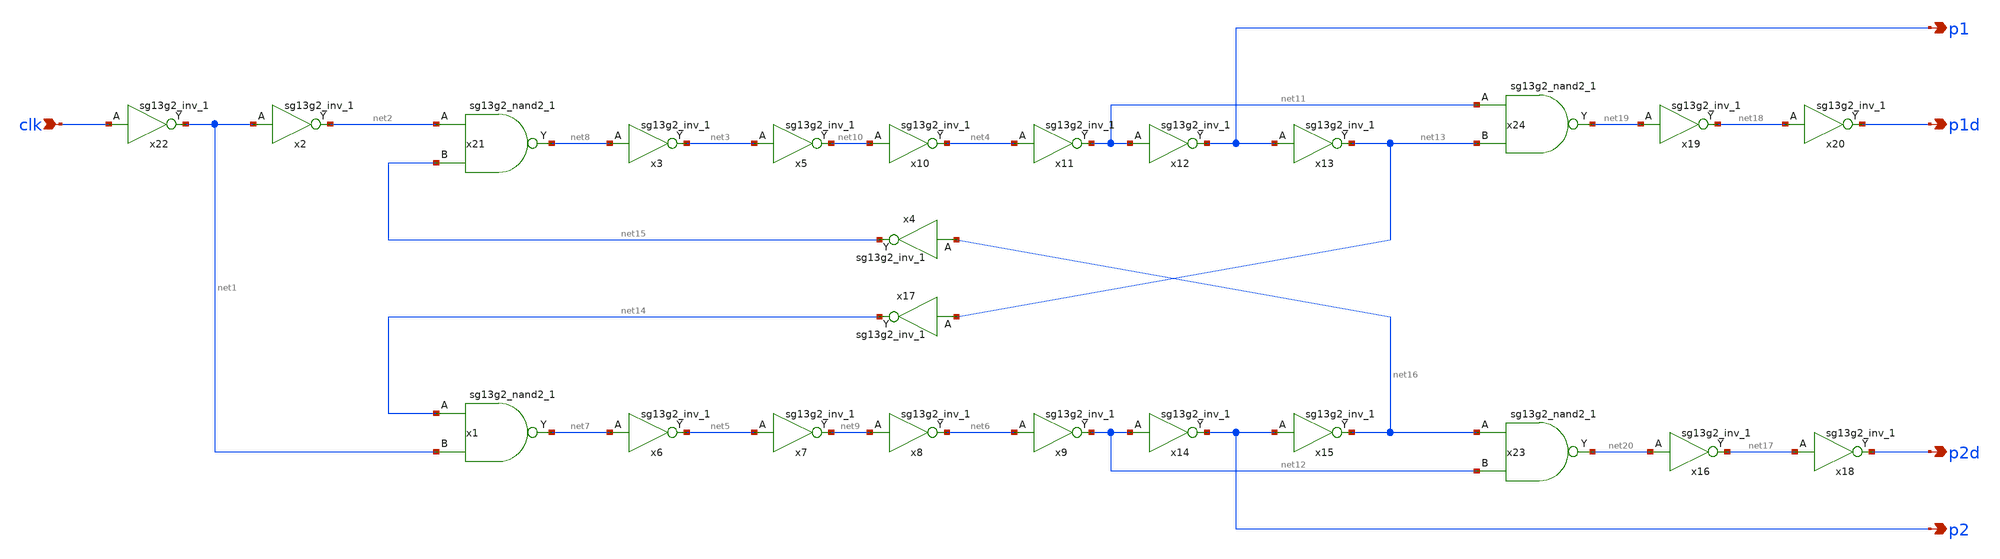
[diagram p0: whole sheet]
** sch_path: design/design_clkgen/clkgen.sch
**.subckt clkgen clk p1 p1d p2d p2
*.ipin clk
*.opin p1
*.opin p1d
*.opin p2d
*.opin p2
x21 net8 net2 net15 VDD VSS sg13g2_nand2_1
x22 net1 clk VDD VSS sg13g2_inv_1
x2 net2 net1 VDD VSS sg13g2_inv_1
x3 net3 net8 VDD VSS sg13g2_inv_1
x5 net10 net3 VDD VSS sg13g2_inv_1
x6 net5 net7 VDD VSS sg13g2_inv_1
x7 net9 net5 VDD VSS sg13g2_inv_1
x8 net6 net9 VDD VSS sg13g2_inv_1
x9 net12 net6 VDD VSS sg13g2_inv_1
x10 net4 net10 VDD VSS sg13g2_inv_1
x11 net11 net4 VDD VSS sg13g2_inv_1
x12 p1 net11 VDD VSS sg13g2_inv_1
x13 net13 p1 VDD VSS sg13g2_inv_1
x14 p2 net12 VDD VSS sg13g2_inv_1
x15 net16 p2 VDD VSS sg13g2_inv_1
x16 net17 net20 VDD VSS sg13g2_inv_1
x18 p2d net17 VDD VSS sg13g2_inv_1
x19 net18 net19 VDD VSS sg13g2_inv_1
x20 p1d net18 VDD VSS sg13g2_inv_1
x4 net15 net16 VDD VSS sg13g2_inv_1
x17 net14 net13 VDD VSS sg13g2_inv_1
x1 net7 net14 net1 VDD VSS sg13g2_nand2_1
x23 net20 net16 net12 VDD VSS sg13g2_nand2_1
x24 net19 net11 net13 VDD VSS sg13g2_nand2_1
**.ends

* expanding   symbol:  sg13g2_stdcells/sg13g2_nand2_1.sym # of pins=3
** sym_path: sg13g2_stdcells/sg13g2_nand2_1.sym
** sch_path: sg13g2_stdcells/sg13g2_nand2_1.sch
.subckt sg13g2_nand2_1 Y A B VDD VSS
*.iopin VDD
*.iopin VSS
*.ipin A
*.ipin B
*.opin Y
XM1 Y A net1 VSS sg13_lv_nmos w=740.00n l=130.00n ng=1 m=1 mm_ok=1
XM2 net1 B VSS VSS sg13_lv_nmos w=740.00n l=130.00n ng=1 m=1 mm_ok=1
XM3 Y A VDD VDD sg13_lv_pmos w=1.12u l=130.00n ng=1 m=1 mm_ok=1
XM4 Y B VDD VDD sg13_lv_pmos w=1.12u l=130.00n ng=1 m=1 mm_ok=1
.ends


* expanding   symbol:  sg13g2_stdcells/sg13g2_inv_1.sym # of pins=2
** sym_path: sg13g2_stdcells/sg13g2_inv_1.sym
** sch_path: sg13g2_stdcells/sg13g2_inv_1.sch
.subckt sg13g2_inv_1 Y A VDD VSS
*.opin Y
*.ipin A
*.iopin VDD
*.iopin VSS
XM1 Y A VSS VSS sg13_lv_nmos w=740.00n l=130.00n ng=1 m=1 mm_ok=1
XM2 Y A VDD VDD sg13_lv_pmos w=1.12u l=130.00n ng=1 m=1 mm_ok=1
.ends

.end
